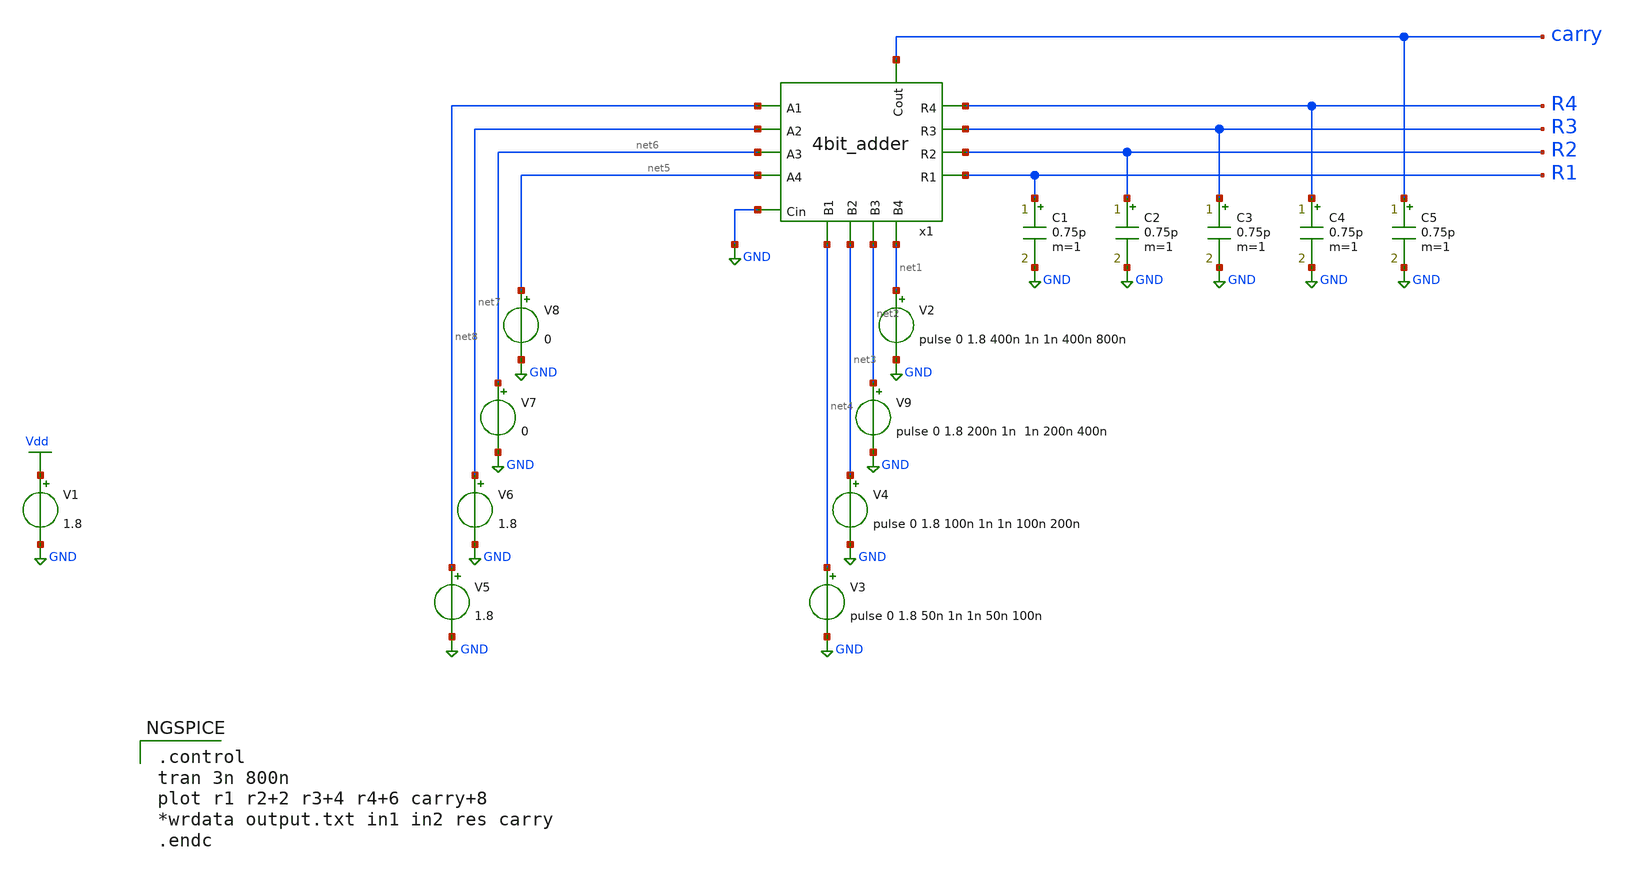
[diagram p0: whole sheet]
** sch_path: Circuiti/adder.sch
**.subckt adder
V1 Vdd GND 1.8
V3 net4 GND pulse 0 1.8 50n 1n 1n 50n 100n
V4 net3 GND pulse 0 1.8 100n 1n 1n 100n 200n
V9 net2 GND pulse 0 1.8 200n 1n 1n 200n 400n
V2 net1 GND pulse 0 1.8 400n 1n 1n 400n 800n
x1 GND net7 net6 net8 net5 net4 net1 net3 net2 carry R4 R3 R2 R1 4bit_adder
V5 net8 GND 1.8
V6 net7 GND 1.8
V7 net6 GND 0
V8 net5 GND 0
C1 R1 GND 0.75p m=1
C2 R2 GND 0.75p m=1
C3 R3 GND 0.75p m=1
C4 R4 GND 0.75p m=1
C5 carry GND 0.75p m=1
**** begin user architecture code


.lib /home/matteo/xschem_downloads/skywater-pdk/libraries/sky130_fd_pr_ngspice/latest/models/sky130.lib.spice tt

*.include /home/matteo/xschem_downloads/skywater-pdk/libraries/sky130_fd_pr_ngspice/latest/cells/nfet_01v8/sky130_fd_pr__nfet_01v8__tt.corner.spice

.param mc_mm_switch=0
.param mc_pr_switch=1



.control
tran 3n 800n
plot r1 r2+2 r3+4 r4+6 carry+8
*wrdata output.txt in1 in2 res carry
.endc



.ic v(r1)=0
.ic v(r2)=0
.ic v(r3)=0
.ic v(r4)=0

**** end user architecture code
**.ends
.GLOBAL GND
.GLOBAL Vdd
.end
